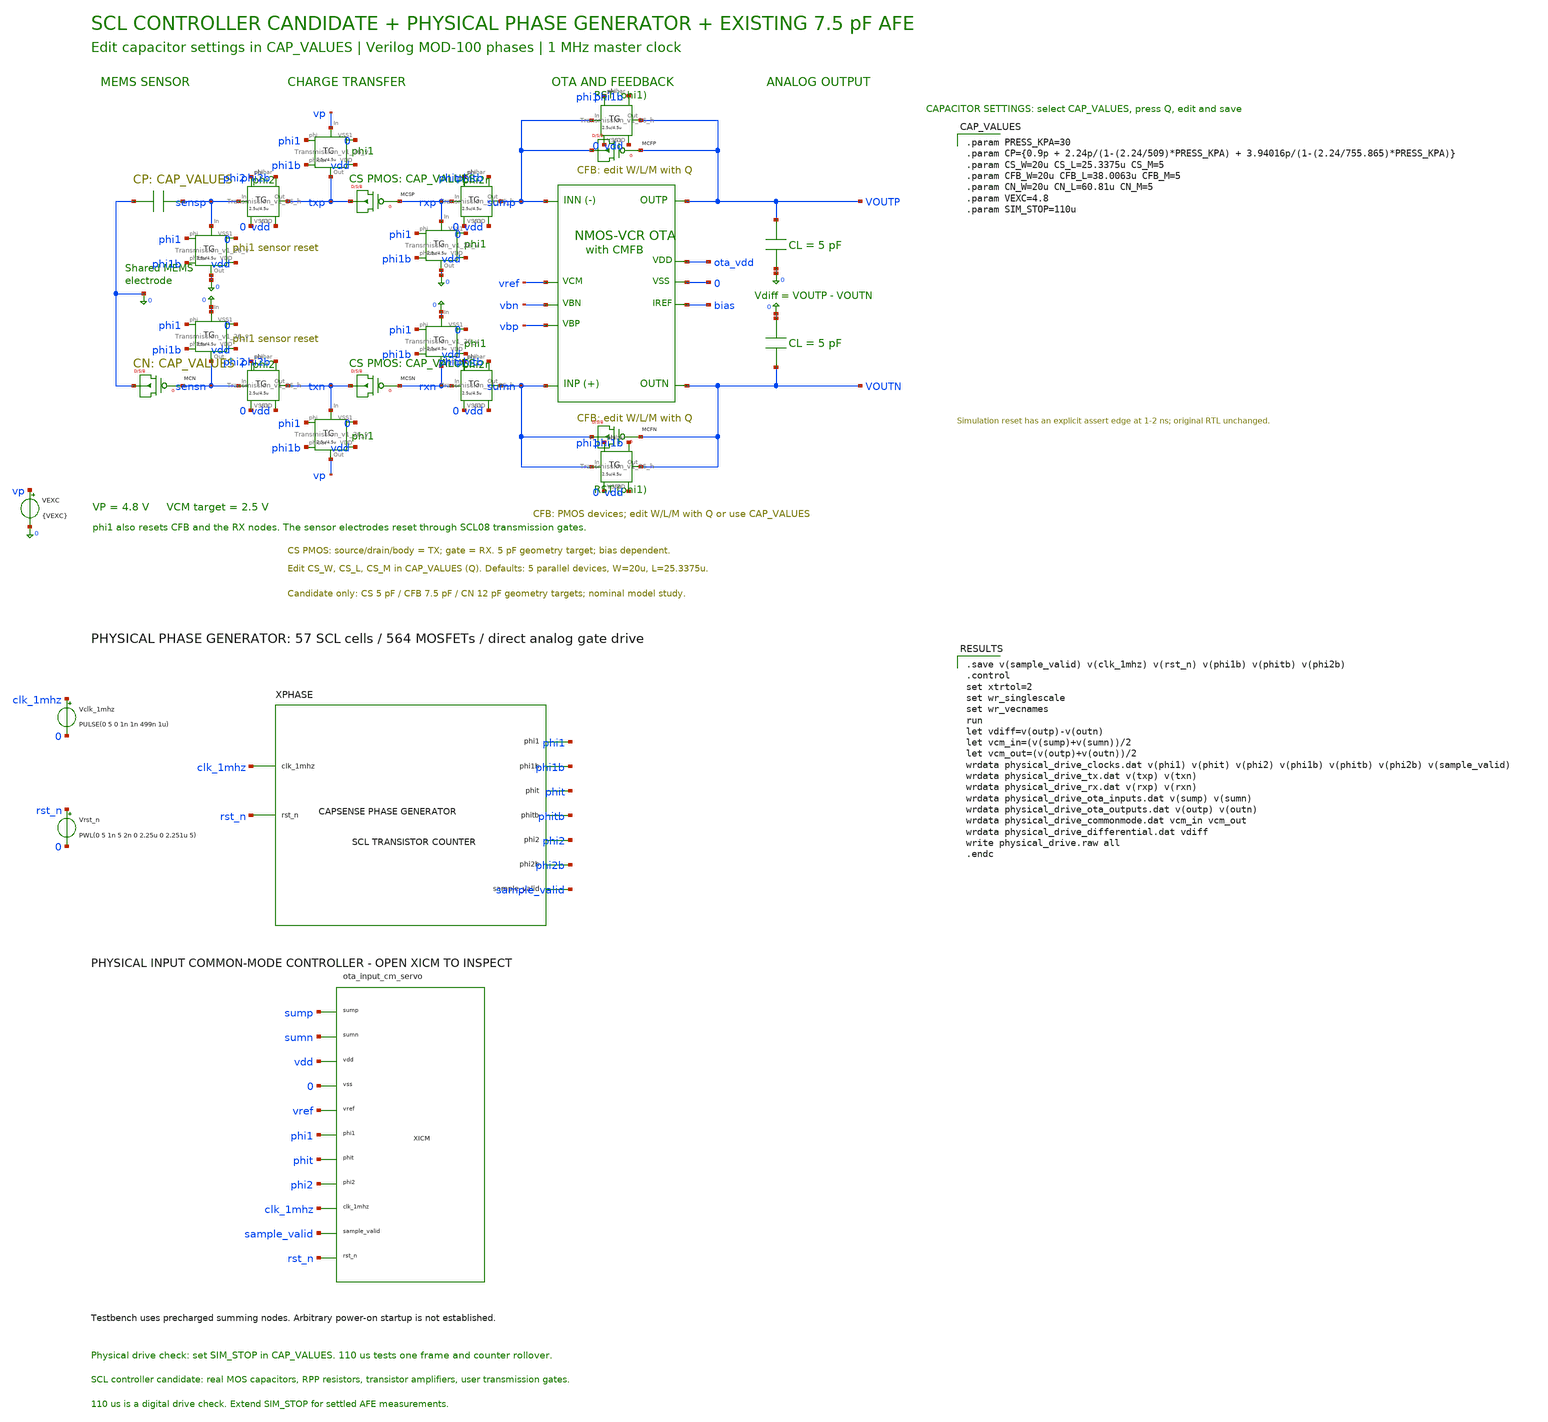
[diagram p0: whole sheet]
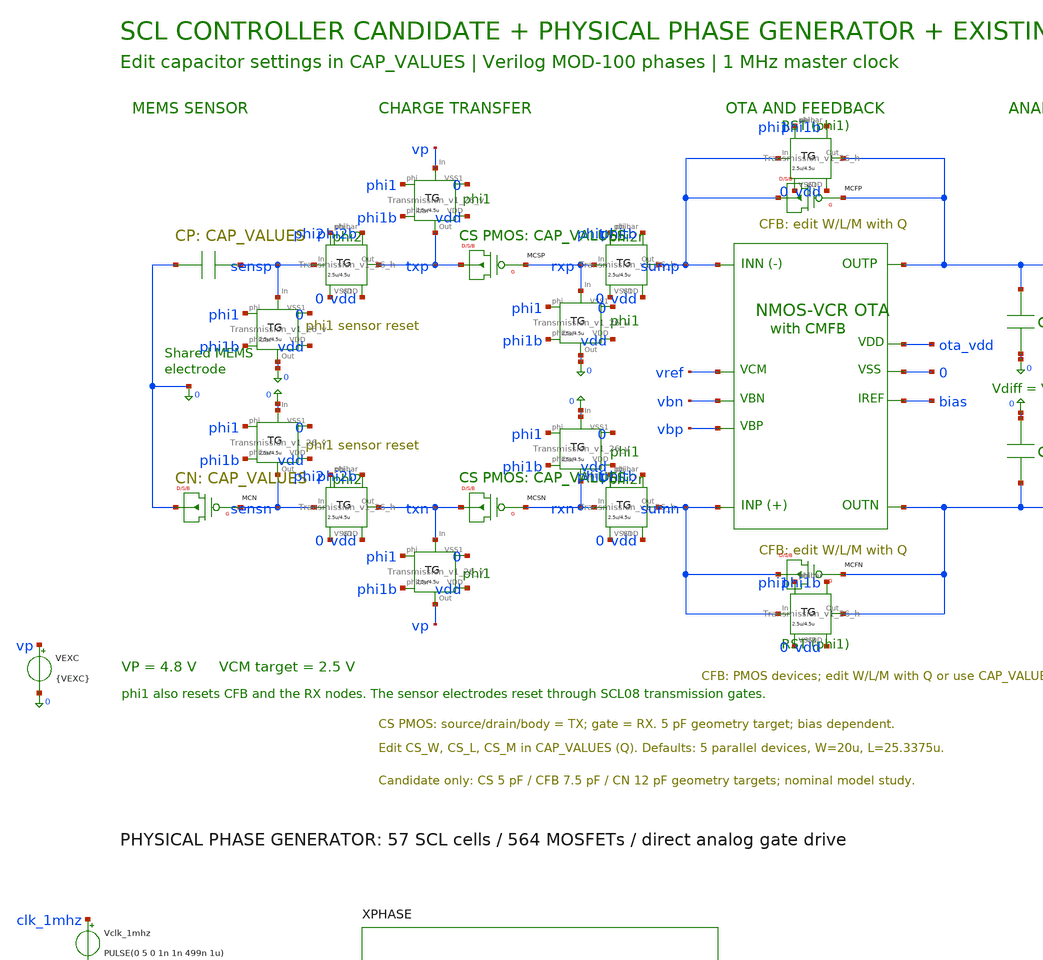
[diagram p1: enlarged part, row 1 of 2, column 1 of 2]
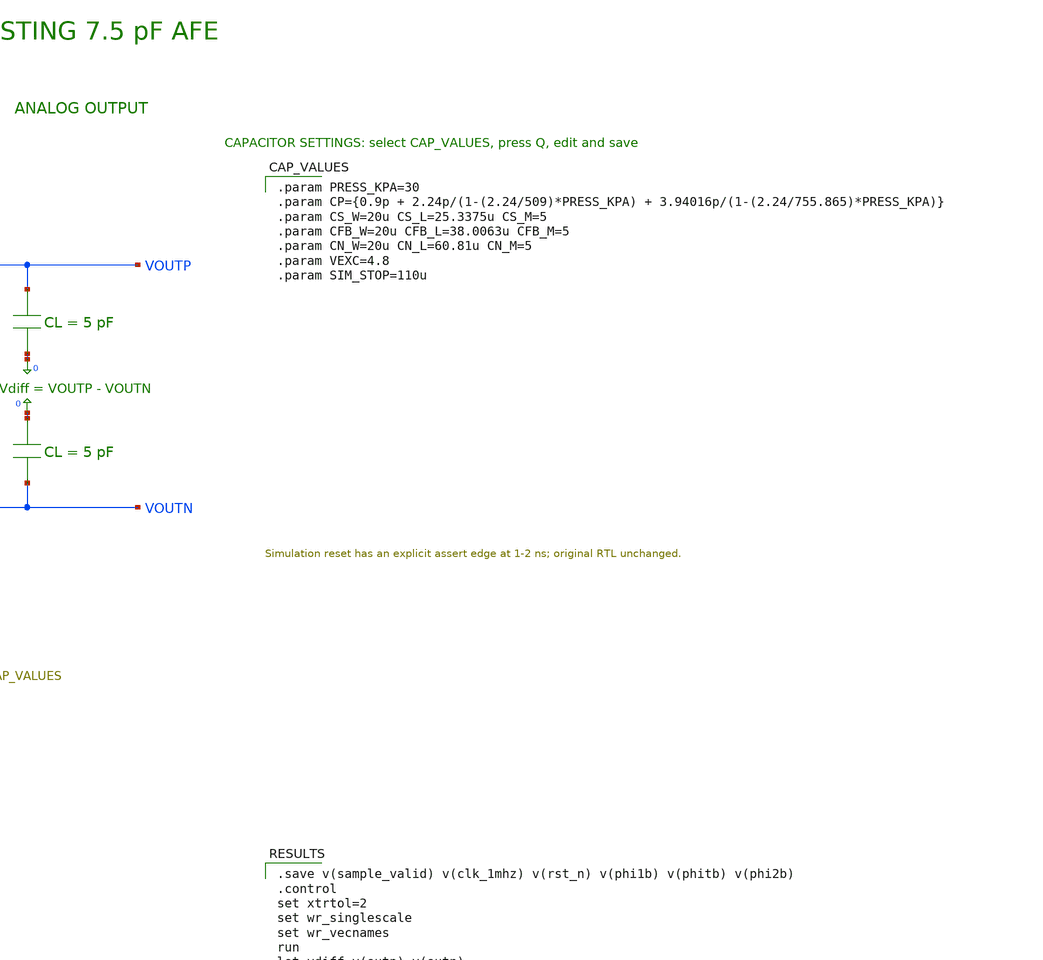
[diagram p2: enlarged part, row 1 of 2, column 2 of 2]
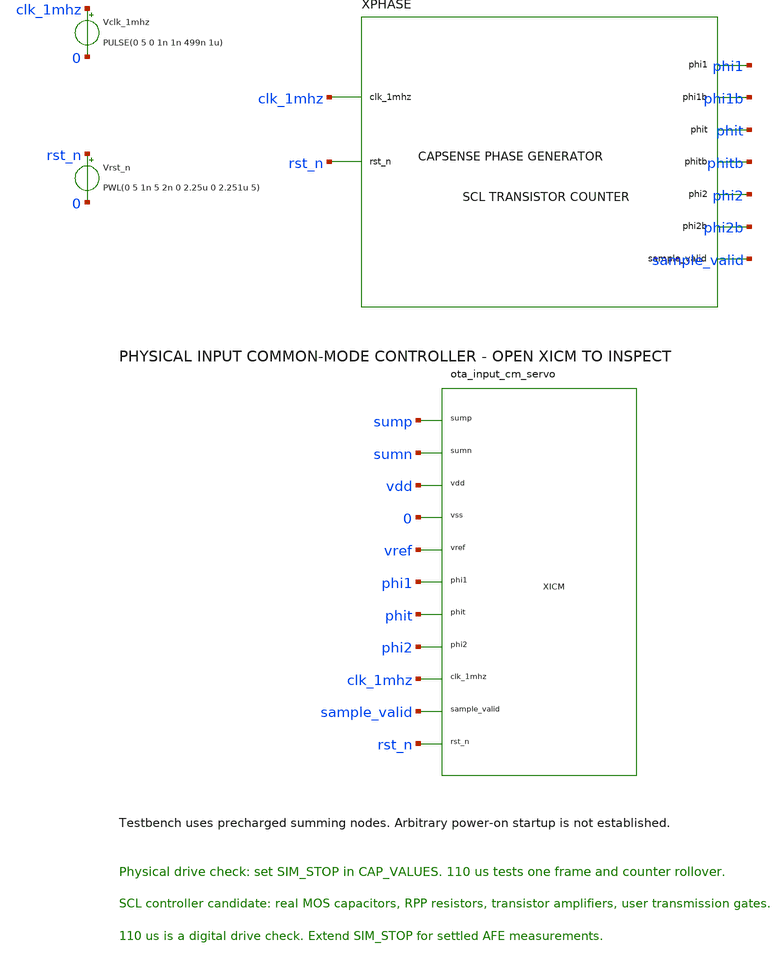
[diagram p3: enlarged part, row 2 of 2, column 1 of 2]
** sch_path: finalv1/schematic/controller/capsense_cfb7p5_scl_controller_tb.sch
**.subckt capsense_cfb7p5_scl_controller_tb
XOTA sumn sump outp outn ota_vdd 0 bias vref vbn vbp ota_telescopic_cm2p5
CMEMP 0 sensp {CP}
XSENSEP phi2 0 sensp txp vdd phi2b Transmission_v1_26_h
XSRESETP phi1 0 sensp 0 vdd phi1b Transmission_v1_26_v
XCHARGEP phi1 0 vp txp vdd phi1b Transmission_v1_26_v
MCSP txp rxp txp txp P W={CS_W} L={CS_L} M={CS_M} AD='( {CS_W} ) * 4.5u' AS='( {CS_W} ) * 4.5u' PD='2 * ( {CS_W} ) + 9u'
+ PS='2 * ( {CS_W} ) + 9u'
XRRESETP phi1 0 rxp 0 vdd phi1b Transmission_v1_26_v
XXFERP phit 0 rxp sump vdd phitb Transmission_v1_26_h
MCFP sump outp sump sump P W={CFB_W} L={CFB_L} M={CFB_M} AD='( {CFB_W} ) * 4.5u' AS='( {CFB_W} ) * 4.5u'
+ PD='2 * ( {CFB_W} ) + 9u' PS='2 * ( {CFB_W} ) + 9u'
XFBRESETP phi1 0 sump outp vdd phi1b Transmission_v1_26_h
CLP outp 0 5p
MCN 0 sensn 0 0 P W={CN_W} L={CN_L} M={CN_M} AD='( {CN_W} ) * 4.5u' AS='( {CN_W} ) * 4.5u' PD='2 * ( {CN_W} ) + 9u'
+ PS='2 * ( {CN_W} ) + 9u'
XSENSEN phi2 0 sensn txn vdd phi2b Transmission_v1_26_h
XSRESETN phi1 0 0 sensn vdd phi1b Transmission_v1_26_v
XCHARGEN phi1 0 txn vp vdd phi1b Transmission_v1_26_v
MCSN txn rxn txn txn P W={CS_W} L={CS_L} M={CS_M} AD='( {CS_W} ) * 4.5u' AS='( {CS_W} ) * 4.5u' PD='2 * ( {CS_W} ) + 9u'
+ PS='2 * ( {CS_W} ) + 9u'
XRRESETN phi1 0 0 rxn vdd phi1b Transmission_v1_26_v
XXFERN phit 0 rxn sumn vdd phitb Transmission_v1_26_h
MCFN sumn outn sumn sumn P W={CFB_W} L={CFB_L} M={CFB_M} AD='( {CFB_W} ) * 4.5u' AS='( {CFB_W} ) * 4.5u'
+ PD='2 * ( {CFB_W} ) + 9u' PS='2 * ( {CFB_W} ) + 9u'
XFBRESETN phi1 0 sumn outn vdd phi1b Transmission_v1_26_h
CLN 0 outn 5p
XPHASE clk_1mhz rst_n phi1 phit phi2 phi1b phitb phi2b sample_valid 0 vdd phase_generator_physical
Vclk_1mhz clk_1mhz 0 PULSE(0 5 0 1n 1n 499n 1u)
Vrst_n rst_n 0 PWL(0 5 1n 5 2n 0 2.25u 0 2.251u 5)
VEXC vp 0 {VEXC}
XICM sump sumn vdd 0 vref phi1 phit phi2 clk_1mhz sample_valid rst_n ota_input_cm_servo
**** begin user architecture code

.include /home/shreyas/open_source_scl_cp8d/open_pdks/scl_cp8d/libs.tech/ngpsice/model/hspice/models49/mos/tntp49_5v
.include /home/shreyas/open_source_scl_cp8d/open_pdks/scl_cp8d/libs.tech/ngpsice/model/hspice/models49/res/typ/ppr
.include ../../models/vcr_low_total.spice
.temp 27
.options reltol=4e-4 vntol=3u abstol=1e-11 numdgt=12 method=gear maxord=2
VDD vdd 0 5
VOTA vdd ota_vdd 0
VREFSRC ref_src 0 2.5
VREFSENSE ref_src vref 0
.include ../../models/clock.spice
.include ../../models/vcr_low_total_bias.spice
VBIASDD vdd bias_vdd 0
XB ref_src bias_vdd 0 vbn vbp bias_src ota_bias08
VIREF bias_src bias 0
RLEAKP sensp 0 1e12
RLEAKN sensn 0 1e12
.save v(outp) v(outn) v(sump) v(sumn) v(txp) v(txn) v(rxp) v(rxn) v(sensp) v(sensn) v(phi1) v(phi2) v(phit) i(vdd) v(vbn) v(vbp) i(viref) i(vota) i(vbiasdd) i(vexc) v(xicm.xcore.cm_x) v(xicm.xcore.cm_hold)
.options method=gear reltol=4e-4 trtol=10
.tran 200n {SIM_STOP} 0 200n
.subckt corrected_tg A B PHI PHIB VDD VSS
MN A PHI B VSS N W=10u L=0.8u AD=45p AS=45p PD=29u PS=29u
MP A PHIB B VDD P W=20u L=0.8u AD=90p AS=90p PD=49u PS=49u
.ends corrected_tg

.subckt user_tg_control A B CTRL VDD
MINV_N cb CTRL 0 0 N W=2.5u L=.8u
MINV_P cb CTRL VDD VDD P W=4.5u L=.8u
XSW CTRL 0 A B VDD cb Transmission_v1_26
.ends user_tg_control

.options klu

.options maxord=2
.ic v(sump)=2.5 v(sumn)=2.5 v(outp)=2.5 v(outn)=2.5 v(rxp)=0 v(rxn)=0 v(txp)=4.8 v(txn)=4.8

.include ../../models/used_scl_cells.spice
.include ../../models/phase_generator_physical.spice


.save v(sample_valid) v(clk_1mhz) v(rst_n) v(phi1b) v(phitb) v(phi2b)
.control
set xtrtol=2
set wr_singlescale
set wr_vecnames
run
let vdiff=v(outp)-v(outn)
let vcm_in=(v(sump)+v(sumn))/2
let vcm_out=(v(outp)+v(outn))/2
wrdata physical_drive_clocks.dat v(phi1) v(phit) v(phi2) v(phi1b) v(phitb) v(phi2b) v(sample_valid)
wrdata physical_drive_tx.dat v(txp) v(txn)
wrdata physical_drive_rx.dat v(rxp) v(rxn)
wrdata physical_drive_ota_inputs.dat v(sump) v(sumn)
wrdata physical_drive_ota_outputs.dat v(outp) v(outn)
wrdata physical_drive_commonmode.dat vcm_in vcm_out
wrdata physical_drive_differential.dat vdiff
write physical_drive.raw all
.endc


.param PRESS_KPA=30
.param CP={0.9p + 2.24p/(1-(2.24/509)*PRESS_KPA) + 3.94016p/(1-(2.24/755.865)*PRESS_KPA)}
.param CS_W=20u CS_L=25.3375u CS_M=5
.param CFB_W=20u CFB_L=38.0063u CFB_M=5
.param CN_W=20u CN_L=60.81u CN_M=5
.param VEXC=4.8
.param SIM_STOP=110u

**** end user architecture code
**.ends
.end
